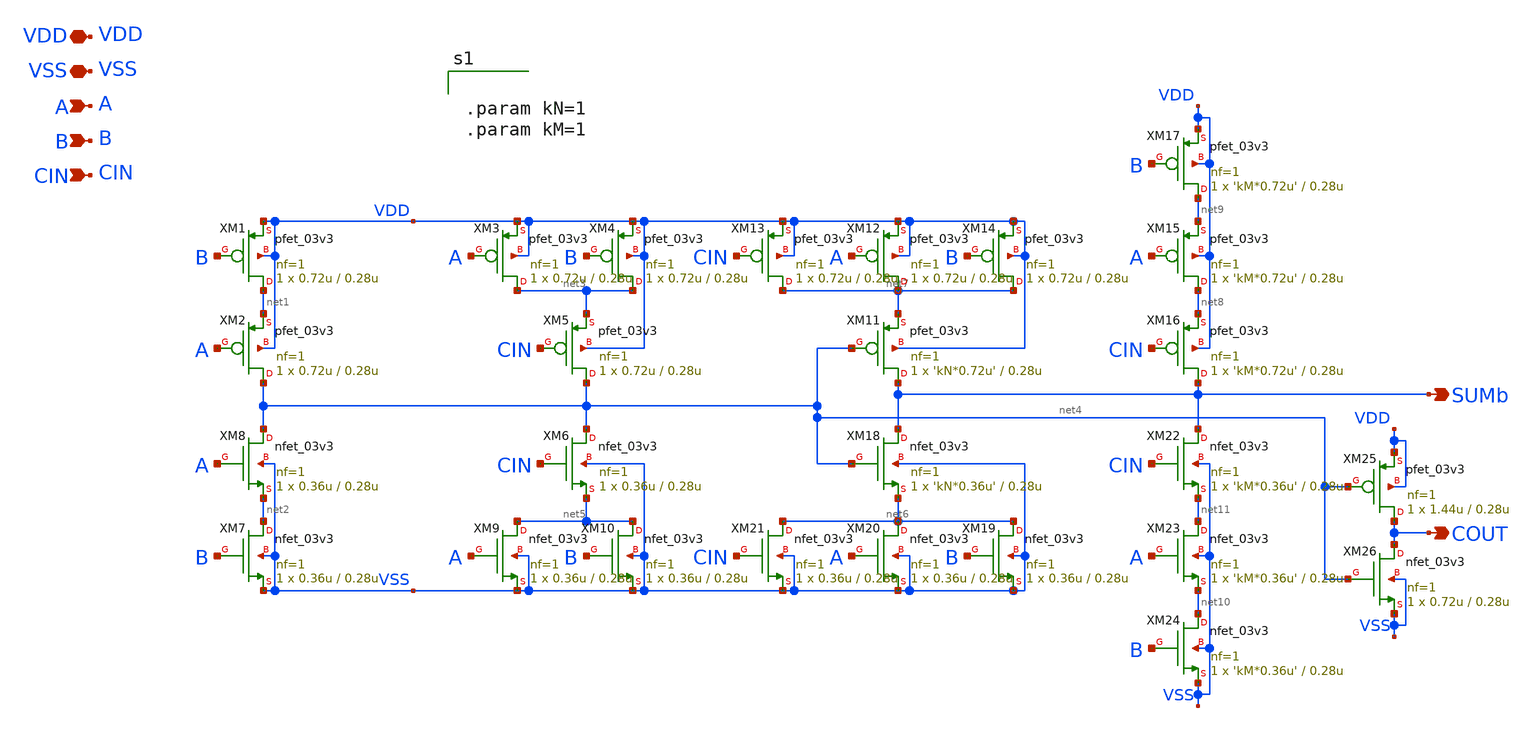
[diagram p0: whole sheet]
** sch_path: CAD4/full_adder.sch
**.subckt full_adder VDD VSS A B CIN SUMb COUT
*.iopin VDD
*.iopin VSS
*.ipin A
*.ipin B
*.ipin CIN
*.opin SUMb
*.opin COUT
XM1 net1 B VDD VDD pfet_03v3 L=0.28u W=0.72u nf=1 ad='int((nf+1)/2) * W/nf * 0.18u' as='int((nf+2)/2) * W/nf * 0.18u'
+ pd='2*int((nf+1)/2) * (W/nf + 0.18u)' ps='2*int((nf+2)/2) * (W/nf + 0.18u)' nrd='0.18u / W' nrs='0.18u / W'
+ sa=0 sb=0 sd=0 m=1
XM2 net4 A net1 VDD pfet_03v3 L=0.28u W=0.72u nf=1 ad='int((nf+1)/2) * W/nf * 0.18u' as='int((nf+2)/2) * W/nf * 0.18u'
+ pd='2*int((nf+1)/2) * (W/nf + 0.18u)' ps='2*int((nf+2)/2) * (W/nf + 0.18u)' nrd='0.18u / W' nrs='0.18u / W'
+ sa=0 sb=0 sd=0 m=1
XM3 net3 A VDD VDD pfet_03v3 L=0.28u W=0.72u nf=1 ad='int((nf+1)/2) * W/nf * 0.18u' as='int((nf+2)/2) * W/nf * 0.18u'
+ pd='2*int((nf+1)/2) * (W/nf + 0.18u)' ps='2*int((nf+2)/2) * (W/nf + 0.18u)' nrd='0.18u / W' nrs='0.18u / W'
+ sa=0 sb=0 sd=0 m=1
XM4 net3 B VDD VDD pfet_03v3 L=0.28u W=0.72u nf=1 ad='int((nf+1)/2) * W/nf * 0.18u' as='int((nf+2)/2) * W/nf * 0.18u'
+ pd='2*int((nf+1)/2) * (W/nf + 0.18u)' ps='2*int((nf+2)/2) * (W/nf + 0.18u)' nrd='0.18u / W' nrs='0.18u / W'
+ sa=0 sb=0 sd=0 m=1
XM5 net4 CIN net3 VDD pfet_03v3 L=0.28u W=0.72u nf=1 ad='int((nf+1)/2) * W/nf * 0.18u' as='int((nf+2)/2) * W/nf * 0.18u'
+ pd='2*int((nf+1)/2) * (W/nf + 0.18u)' ps='2*int((nf+2)/2) * (W/nf + 0.18u)' nrd='0.18u / W' nrs='0.18u / W'
+ sa=0 sb=0 sd=0 m=1
XM6 net4 CIN net5 VSS nfet_03v3 L=0.28u W=0.36u nf=1 ad='int((nf+1)/2) * W/nf * 0.18u' as='int((nf+2)/2) * W/nf * 0.18u'
+ pd='2*int((nf+1)/2) * (W/nf + 0.18u)' ps='2*int((nf+2)/2) * (W/nf + 0.18u)' nrd='0.18u / W' nrs='0.18u / W'
+ sa=0 sb=0 sd=0 m=1
XM7 net2 B VSS VSS nfet_03v3 L=0.28u W=0.36u nf=1 ad='int((nf+1)/2) * W/nf * 0.18u' as='int((nf+2)/2) * W/nf * 0.18u'
+ pd='2*int((nf+1)/2) * (W/nf + 0.18u)' ps='2*int((nf+2)/2) * (W/nf + 0.18u)' nrd='0.18u / W' nrs='0.18u / W'
+ sa=0 sb=0 sd=0 m=1
XM8 net4 A net2 VSS nfet_03v3 L=0.28u W=0.36u nf=1 ad='int((nf+1)/2) * W/nf * 0.18u' as='int((nf+2)/2) * W/nf * 0.18u'
+ pd='2*int((nf+1)/2) * (W/nf + 0.18u)' ps='2*int((nf+2)/2) * (W/nf + 0.18u)' nrd='0.18u / W' nrs='0.18u / W'
+ sa=0 sb=0 sd=0 m=1
XM9 net5 A VSS VSS nfet_03v3 L=0.28u W=0.36u nf=1 ad='int((nf+1)/2) * W/nf * 0.18u' as='int((nf+2)/2) * W/nf * 0.18u'
+ pd='2*int((nf+1)/2) * (W/nf + 0.18u)' ps='2*int((nf+2)/2) * (W/nf + 0.18u)' nrd='0.18u / W' nrs='0.18u / W'
+ sa=0 sb=0 sd=0 m=1
XM10 net5 B VSS VSS nfet_03v3 L=0.28u W=0.36u nf=1 ad='int((nf+1)/2) * W/nf * 0.18u' as='int((nf+2)/2) * W/nf * 0.18u'
+ pd='2*int((nf+1)/2) * (W/nf + 0.18u)' ps='2*int((nf+2)/2) * (W/nf + 0.18u)' nrd='0.18u / W' nrs='0.18u / W'
+ sa=0 sb=0 sd=0 m=1
XM11 SUMb net4 net7 VDD pfet_03v3 L=0.28u W='kN*0.72u' nf=1 ad='int((nf+1)/2) * W/nf * 0.18u' as='int((nf+2)/2) * W/nf * 0.18u'
+ pd='2*int((nf+1)/2) * (W/nf + 0.18u)' ps='2*int((nf+2)/2) * (W/nf + 0.18u)' nrd='0.18u / W' nrs='0.18u / W'
+ sa=0 sb=0 sd=0 m=1
XM12 net7 A VDD VDD pfet_03v3 L=0.28u W=0.72u nf=1 ad='int((nf+1)/2) * W/nf * 0.18u' as='int((nf+2)/2) * W/nf * 0.18u'
+ pd='2*int((nf+1)/2) * (W/nf + 0.18u)' ps='2*int((nf+2)/2) * (W/nf + 0.18u)' nrd='0.18u / W' nrs='0.18u / W'
+ sa=0 sb=0 sd=0 m=1
XM13 net7 CIN VDD VDD pfet_03v3 L=0.28u W=0.72u nf=1 ad='int((nf+1)/2) * W/nf * 0.18u' as='int((nf+2)/2) * W/nf * 0.18u'
+ pd='2*int((nf+1)/2) * (W/nf + 0.18u)' ps='2*int((nf+2)/2) * (W/nf + 0.18u)' nrd='0.18u / W' nrs='0.18u / W'
+ sa=0 sb=0 sd=0 m=1
XM14 net7 B VDD VDD pfet_03v3 L=0.28u W=0.72u nf=1 ad='int((nf+1)/2) * W/nf * 0.18u' as='int((nf+2)/2) * W/nf * 0.18u'
+ pd='2*int((nf+1)/2) * (W/nf + 0.18u)' ps='2*int((nf+2)/2) * (W/nf + 0.18u)' nrd='0.18u / W' nrs='0.18u / W'
+ sa=0 sb=0 sd=0 m=1
XM15 net8 A net9 VDD pfet_03v3 L=0.28u W='kM*0.72u' nf=1 ad='int((nf+1)/2) * W/nf * 0.18u' as='int((nf+2)/2) * W/nf * 0.18u'
+ pd='2*int((nf+1)/2) * (W/nf + 0.18u)' ps='2*int((nf+2)/2) * (W/nf + 0.18u)' nrd='0.18u / W' nrs='0.18u / W'
+ sa=0 sb=0 sd=0 m=1
XM16 SUMb CIN net8 VDD pfet_03v3 L=0.28u W='kM*0.72u' nf=1 ad='int((nf+1)/2) * W/nf * 0.18u' as='int((nf+2)/2) * W/nf * 0.18u'
+ pd='2*int((nf+1)/2) * (W/nf + 0.18u)' ps='2*int((nf+2)/2) * (W/nf + 0.18u)' nrd='0.18u / W' nrs='0.18u / W'
+ sa=0 sb=0 sd=0 m=1
XM17 net9 B VDD VDD pfet_03v3 L=0.28u W='kM*0.72u' nf=1 ad='int((nf+1)/2) * W/nf * 0.18u' as='int((nf+2)/2) * W/nf * 0.18u'
+ pd='2*int((nf+1)/2) * (W/nf + 0.18u)' ps='2*int((nf+2)/2) * (W/nf + 0.18u)' nrd='0.18u / W' nrs='0.18u / W'
+ sa=0 sb=0 sd=0 m=1
XM18 SUMb net4 net6 VSS nfet_03v3 L=0.28u W='kN*0.36u' nf=1 ad='int((nf+1)/2) * W/nf * 0.18u' as='int((nf+2)/2) * W/nf * 0.18u'
+ pd='2*int((nf+1)/2) * (W/nf + 0.18u)' ps='2*int((nf+2)/2) * (W/nf + 0.18u)' nrd='0.18u / W' nrs='0.18u / W'
+ sa=0 sb=0 sd=0 m=1
XM19 net6 B VSS VSS nfet_03v3 L=0.28u W=0.36u nf=1 ad='int((nf+1)/2) * W/nf * 0.18u' as='int((nf+2)/2) * W/nf * 0.18u'
+ pd='2*int((nf+1)/2) * (W/nf + 0.18u)' ps='2*int((nf+2)/2) * (W/nf + 0.18u)' nrd='0.18u / W' nrs='0.18u / W'
+ sa=0 sb=0 sd=0 m=1
XM20 net6 A VSS VSS nfet_03v3 L=0.28u W=0.36u nf=1 ad='int((nf+1)/2) * W/nf * 0.18u' as='int((nf+2)/2) * W/nf * 0.18u'
+ pd='2*int((nf+1)/2) * (W/nf + 0.18u)' ps='2*int((nf+2)/2) * (W/nf + 0.18u)' nrd='0.18u / W' nrs='0.18u / W'
+ sa=0 sb=0 sd=0 m=1
XM21 net6 CIN VSS VSS nfet_03v3 L=0.28u W=0.36u nf=1 ad='int((nf+1)/2) * W/nf * 0.18u' as='int((nf+2)/2) * W/nf * 0.18u'
+ pd='2*int((nf+1)/2) * (W/nf + 0.18u)' ps='2*int((nf+2)/2) * (W/nf + 0.18u)' nrd='0.18u / W' nrs='0.18u / W'
+ sa=0 sb=0 sd=0 m=1
XM22 SUMb CIN net11 VSS nfet_03v3 L=0.28u W='kM*0.36u' nf=1 ad='int((nf+1)/2) * W/nf * 0.18u' as='int((nf+2)/2) * W/nf * 0.18u'
+ pd='2*int((nf+1)/2) * (W/nf + 0.18u)' ps='2*int((nf+2)/2) * (W/nf + 0.18u)' nrd='0.18u / W' nrs='0.18u / W'
+ sa=0 sb=0 sd=0 m=1
XM23 net11 A net10 VSS nfet_03v3 L=0.28u W='kM*0.36u' nf=1 ad='int((nf+1)/2) * W/nf * 0.18u' as='int((nf+2)/2) * W/nf * 0.18u'
+ pd='2*int((nf+1)/2) * (W/nf + 0.18u)' ps='2*int((nf+2)/2) * (W/nf + 0.18u)' nrd='0.18u / W' nrs='0.18u / W'
+ sa=0 sb=0 sd=0 m=1
XM24 net10 B VSS VSS nfet_03v3 L=0.28u W='kM*0.36u' nf=1 ad='int((nf+1)/2) * W/nf * 0.18u' as='int((nf+2)/2) * W/nf * 0.18u'
+ pd='2*int((nf+1)/2) * (W/nf + 0.18u)' ps='2*int((nf+2)/2) * (W/nf + 0.18u)' nrd='0.18u / W' nrs='0.18u / W'
+ sa=0 sb=0 sd=0 m=1
XM25 COUT net4 VDD VDD pfet_03v3 L=0.28u W=1.44u nf=1 ad='int((nf+1)/2) * W/nf * 0.18u' as='int((nf+2)/2) * W/nf * 0.18u'
+ pd='2*int((nf+1)/2) * (W/nf + 0.18u)' ps='2*int((nf+2)/2) * (W/nf + 0.18u)' nrd='0.18u / W' nrs='0.18u / W'
+ sa=0 sb=0 sd=0 m=1
XM26 COUT net4 VSS VSS nfet_03v3 L=0.28u W=0.72u nf=1 ad='int((nf+1)/2) * W/nf * 0.18u' as='int((nf+2)/2) * W/nf * 0.18u'
+ pd='2*int((nf+1)/2) * (W/nf + 0.18u)' ps='2*int((nf+2)/2) * (W/nf + 0.18u)' nrd='0.18u / W' nrs='0.18u / W'
+ sa=0 sb=0 sd=0 m=1
**** begin user architecture code


.param kN=1
.param kM=1


**** end user architecture code
**.ends
.end
